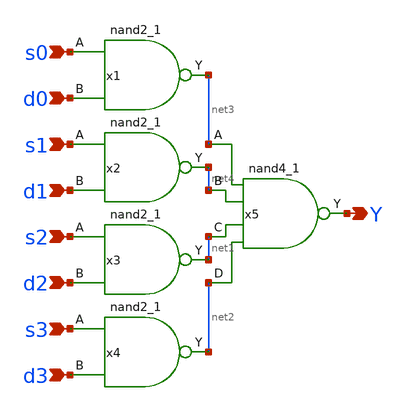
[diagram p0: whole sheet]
** sch_path: elements/mux4.sch
**.subckt mux4 s0 d0 s1 d1 s2 d2 s3 d3 Y
*.ipin s0
*.ipin d0
*.ipin s1
*.ipin d1
*.ipin s2
*.ipin d2
*.ipin s3
*.ipin d3
*.opin Y
x4 s3 d3 VSS VSS VCC VCC net2 sky130_fd_sc_hd__nand2_1
x1 s0 d0 VSS VSS VCC VCC net3 sky130_fd_sc_hd__nand2_1
x2 s1 d1 VSS VSS VCC VCC net4 sky130_fd_sc_hd__nand2_1
x3 s2 d2 VSS VSS VCC VCC net1 sky130_fd_sc_hd__nand2_1
x5 net3 net4 net1 net2 VSS VSS VCC VCC Y sky130_fd_sc_hd__nand4_1
**.ends
.end
